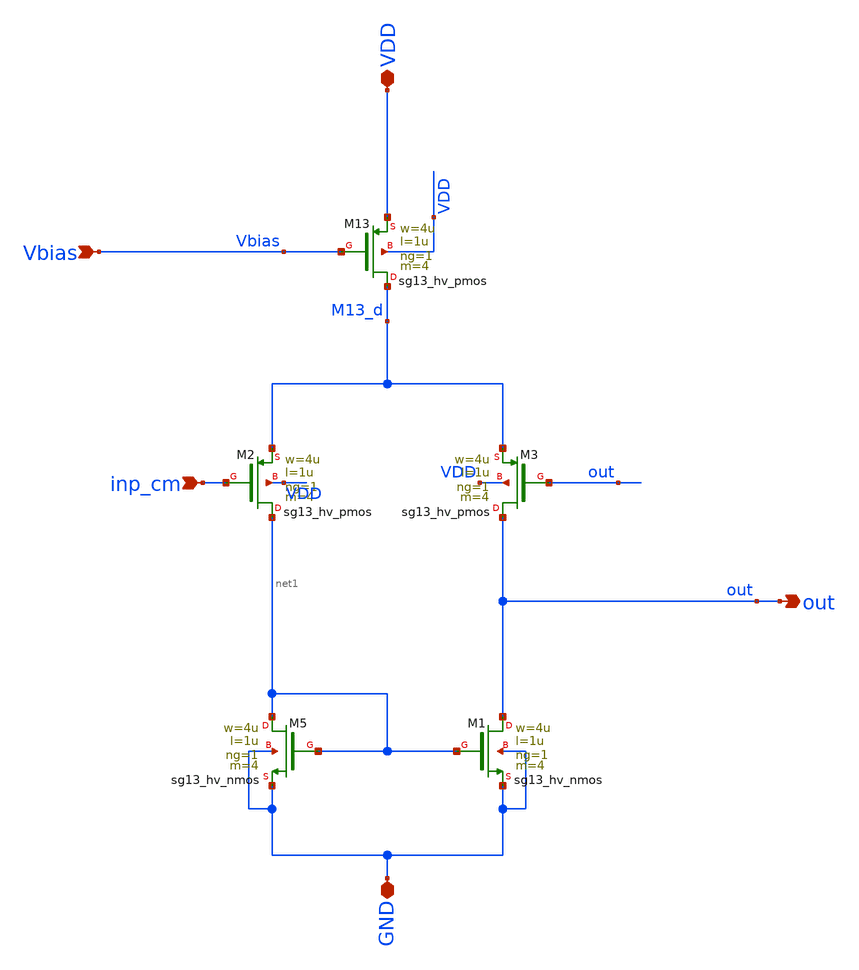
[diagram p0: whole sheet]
** sch_path: xschem/V2I/buffer_final.sch
**.subckt buffer_final inp_cm out VDD GND Vbias
*.ipin inp_cm
*.opin out
*.iopin VDD
*.iopin GND
*.ipin Vbias
XM2 net1 inp_cm M13_d VDD sg13_hv_pmos w=4u l=1u ng=1 m=4 mm_ok=1
XM5 net1 net1 GND GND sg13_hv_nmos w=4u l=1u ng=1 m=4 mm_ok=1
XM13 M13_d Vbias VDD VDD sg13_hv_pmos w=4u l=1u ng=1 m=4 mm_ok=1
XM3 out out M13_d VDD sg13_hv_pmos w=4u l=1u ng=1 m=4 mm_ok=1
XM1 out net1 GND GND sg13_hv_nmos w=4u l=1u ng=1 m=4 mm_ok=1
**.ends
.end
